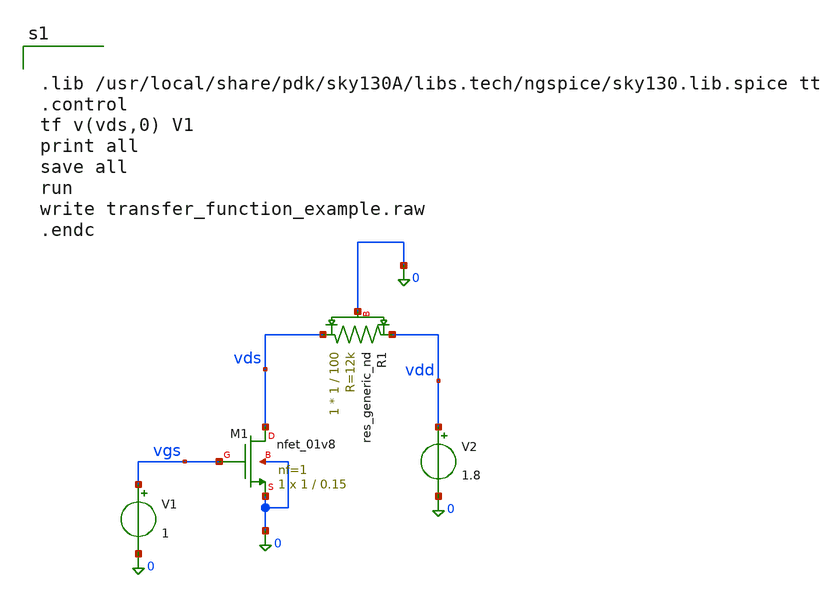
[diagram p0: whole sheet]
** sch_path: mag/transfer_function_example.sch
**.subckt transfer_function_example
V1 vgs 0 1
V2 vdd 0 1.8
XM1 vds vgs 0 0 sky130_fd_pr__nfet_01v8 L=0.15 W=1 nf=1 ad='int((1 + 1)/2) * 1 / 1 * 0.29' as='int((1 + 2)/2) * 1 / 1 * 0.29'
+ pd='2*int((1 + 1)/2) * (1 / 1 + 0.29)' ps='2*int((1 + 2)/2) * (1 / 1 + 0.29)' nrd='0.29 / 1 ' nrs='0.29 / 1 '
+ sa=0 sb=0 sd=0 mult=1 m=1
XR1 vds vdd 0 sky130_fd_pr__res_generic_nd W=1 L=100 mult=1 m=1
**** begin user architecture code


.lib /usr/local/share/pdk/sky130A/libs.tech/ngspice/sky130.lib.spice tt
.control
tf v(vds,0) V1
print all
save all
run
write transfer_function_example.raw
.endc

**** end user architecture code
**.ends
.end
